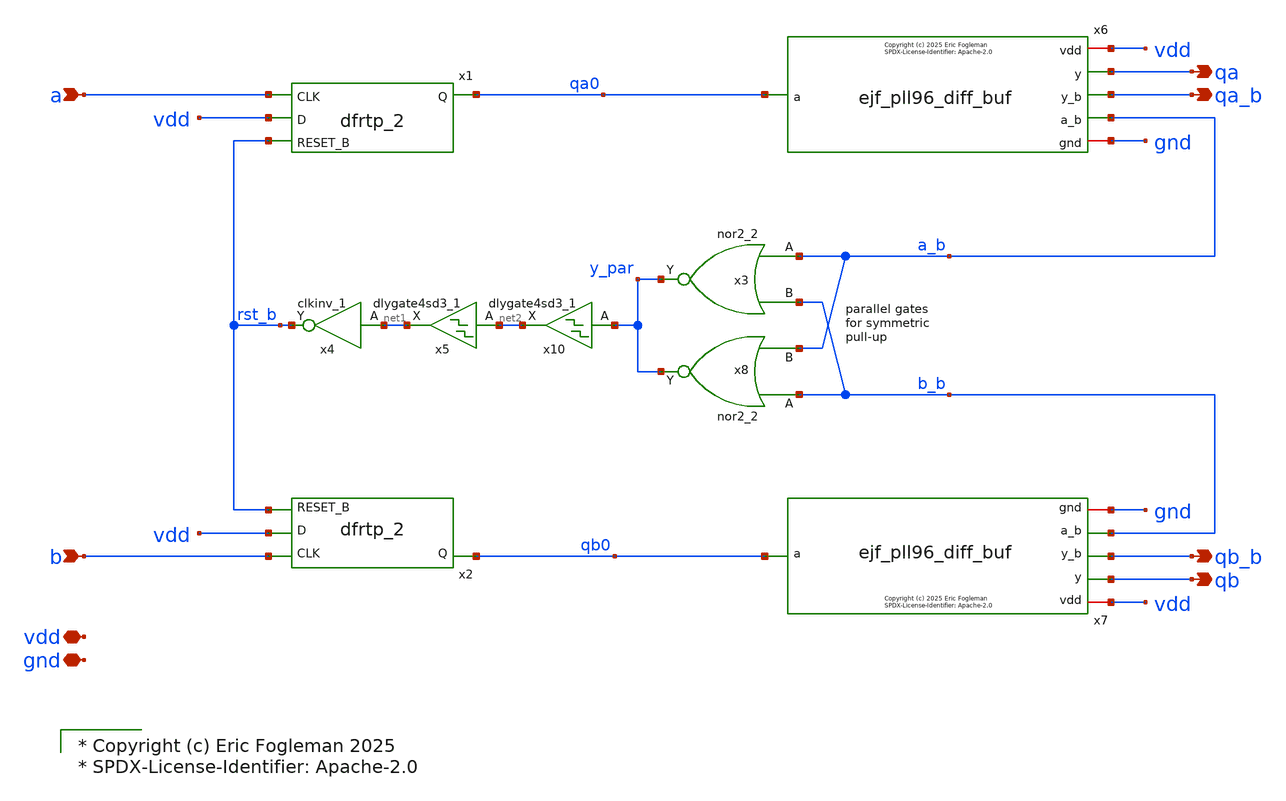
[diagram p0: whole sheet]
** sch_path: xschem/ejf_pll96_pfd.sch
* xschem/ejf_pll96_diff_buf.sym:
* Copyright (c) 2025 Eric Fogleman

* Copyright (c) Eric Fogleman 2025
* SPDX-License-Identifier: Apache-2.0

**.subckt ejf_pll96_pfd vdd gnd a b qa qb qa_b qb_b
*.iopin vdd
*.iopin gnd
*.ipin a
*.ipin b
*.opin qa
*.opin qb
*.opin qa_b
*.opin qb_b
x3 a_b b_b gnd gnd vdd vdd y_par sky130_fd_sc_ls__nor2_2
x4 net1 gnd gnd vdd vdd rst_b sky130_fd_sc_ls__clkinv_1
x1 a vdd rst_b gnd gnd vdd vdd qa0 sky130_fd_sc_ls__dfrtp_2
x2 b vdd rst_b gnd gnd vdd vdd qb0 sky130_fd_sc_ls__dfrtp_2
x6 vdd qa0 qa_b qa gnd a_b ejf_pll96_diff_buf
x7 vdd qb0 qb_b qb gnd b_b ejf_pll96_diff_buf
x8 b_b a_b gnd gnd vdd vdd y_par sky130_fd_sc_ls__nor2_2
x10 y_par gnd gnd vdd vdd net2 sky130_fd_sc_ls__dlygate4sd3_1
x5 net2 gnd gnd vdd vdd net1 sky130_fd_sc_ls__dlygate4sd3_1
**.ends

* expanding   symbol:  ejf_pll96_diff_buf.sym # of pins=6
** sym_path: xschem/ejf_pll96_diff_buf.sym
** sch_path: xschem/ejf_pll96_diff_buf.sch
.subckt ejf_pll96_diff_buf vdd a y_b y gnd a_b
*.iopin vdd
*.iopin gnd
*.ipin a
*.opin y_b
*.opin y
*.opin a_b
XM11 a_b a gnd gnd sky130_fd_pr__nfet_01v8 L=0.15 W=0.84 nf=2 ad='int((nf+1)/2) * W/nf * 0.29' as='int((nf+2)/2) * W/nf * 0.29'
+ pd='2*int((nf+1)/2) * (W/nf + 0.29)' ps='2*int((nf+2)/2) * (W/nf + 0.29)' nrd='0.29 / W' nrs='0.29 / W'
+ sa=0 sb=0 sd=0 mult=1 m=1
XM12 a_b a vdd vdd sky130_fd_pr__pfet_01v8_hvt L=0.15 W=3.36 nf=3 ad='int((nf+1)/2) * W/nf * 0.29' as='int((nf+2)/2) * W/nf * 0.29'
+ pd='2*int((nf+1)/2) * (W/nf + 0.29)' ps='2*int((nf+2)/2) * (W/nf + 0.29)' nrd='0.29 / W' nrs='0.29 / W'
+ sa=0 sb=0 sd=0 mult=1 m=1
XM1 y_b net1 gnd gnd sky130_fd_pr__nfet_01v8 L=0.15 W=0.84 nf=2 ad='int((nf+1)/2) * W/nf * 0.29' as='int((nf+2)/2) * W/nf * 0.29'
+ pd='2*int((nf+1)/2) * (W/nf + 0.29)' ps='2*int((nf+2)/2) * (W/nf + 0.29)' nrd='0.29 / W' nrs='0.29 / W'
+ sa=0 sb=0 sd=0 mult=1 m=1
XM2 y_b net1 vdd vdd sky130_fd_pr__pfet_01v8_hvt L=0.15 W=3.36 nf=3 ad='int((nf+1)/2) * W/nf * 0.29'
+ as='int((nf+2)/2) * W/nf * 0.29' pd='2*int((nf+1)/2) * (W/nf + 0.29)' ps='2*int((nf+2)/2) * (W/nf + 0.29)'
+ nrd='0.29 / W' nrs='0.29 / W' sa=0 sb=0 sd=0 mult=1 m=1
XM3 net1 a_b gnd gnd sky130_fd_pr__nfet_01v8 L=0.15 W=0.84 nf=2 ad='int((nf+1)/2) * W/nf * 0.29' as='int((nf+2)/2) * W/nf * 0.29'
+ pd='2*int((nf+1)/2) * (W/nf + 0.29)' ps='2*int((nf+2)/2) * (W/nf + 0.29)' nrd='0.29 / W' nrs='0.29 / W'
+ sa=0 sb=0 sd=0 mult=1 m=1
XM4 net1 a_b vdd vdd sky130_fd_pr__pfet_01v8_hvt L=0.15 W=3.36 nf=3 ad='int((nf+1)/2) * W/nf * 0.29'
+ as='int((nf+2)/2) * W/nf * 0.29' pd='2*int((nf+1)/2) * (W/nf + 0.29)' ps='2*int((nf+2)/2) * (W/nf + 0.29)'
+ nrd='0.29 / W' nrs='0.29 / W' sa=0 sb=0 sd=0 mult=1 m=1
XM5 y net2 gnd gnd sky130_fd_pr__nfet_01v8 L=0.15 W=0.84 nf=2 ad='int((nf+1)/2) * W/nf * 0.29' as='int((nf+2)/2) * W/nf * 0.29'
+ pd='2*int((nf+1)/2) * (W/nf + 0.29)' ps='2*int((nf+2)/2) * (W/nf + 0.29)' nrd='0.29 / W' nrs='0.29 / W'
+ sa=0 sb=0 sd=0 mult=1 m=1
XM6 y net2 vdd vdd sky130_fd_pr__pfet_01v8_hvt L=0.15 W=3.36 nf=3 ad='int((nf+1)/2) * W/nf * 0.29' as='int((nf+2)/2) * W/nf * 0.29'
+ pd='2*int((nf+1)/2) * (W/nf + 0.29)' ps='2*int((nf+2)/2) * (W/nf + 0.29)' nrd='0.29 / W' nrs='0.29 / W'
+ sa=0 sb=0 sd=0 mult=1 m=1
XM9 net2 gnd a_b VDD sky130_fd_pr__pfet_01v8_hvt L=0.15 W=3.36 nf=3 ad='int((nf+1)/2) * W/nf * 0.29'
+ as='int((nf+2)/2) * W/nf * 0.29' pd='2*int((nf+1)/2) * (W/nf + 0.29)' ps='2*int((nf+2)/2) * (W/nf + 0.29)'
+ nrd='0.29 / W' nrs='0.29 / W' sa=0 sb=0 sd=0 mult=1 m=1
XM10 net2 vdd a_b GND sky130_fd_pr__nfet_01v8 L=0.15 W=0.84 nf=2 ad='int((nf+1)/2) * W/nf * 0.29' as='int((nf+2)/2) * W/nf * 0.29'
+ pd='2*int((nf+1)/2) * (W/nf + 0.29)' ps='2*int((nf+2)/2) * (W/nf + 0.29)' nrd='0.29 / W' nrs='0.29 / W'
+ sa=0 sb=0 sd=0 mult=1 m=1
**** begin user architecture code

* Copyright (c) Eric Fogleman 2025
* SPDX-License-Identifier: Apache-2.0

**** end user architecture code
.ends

.end
